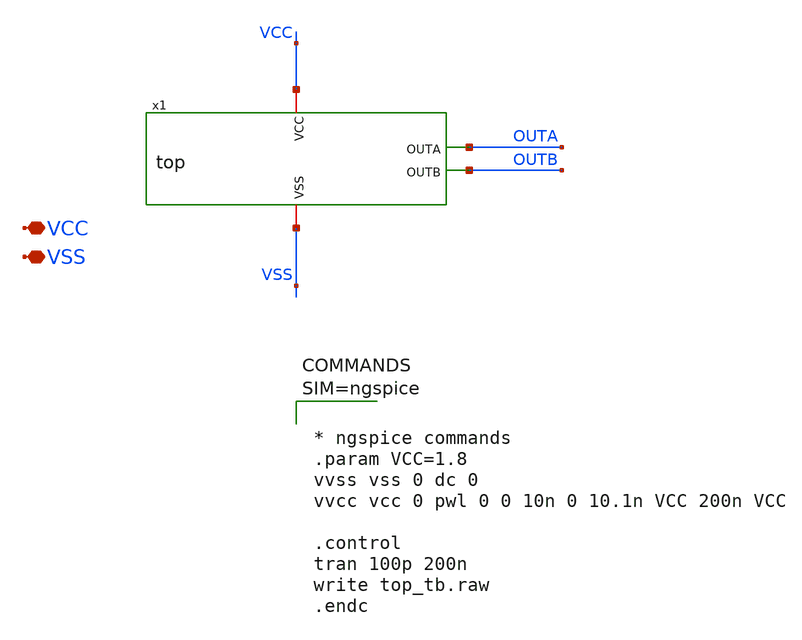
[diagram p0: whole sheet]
** sch_path: xschem/top_tb.sch
**.subckt top_tb VCC VSS
*.iopin VCC
*.iopin VSS
x1 VCC OUTA OUTB VSS top
**** begin user architecture code

** opencircuitdesign pdks install
.lib $::SKYWATER_MODELS/sky130.lib.spice tt





* ngspice commands
.param VCC=1.8
vvss vss 0 dc 0
vvcc vcc 0 pwl 0 0 10n 0 10.1n VCC 200n VCC

.control
tran 100p 200n
write top_tb.raw
.endc




**** end user architecture code
**.ends
.end
